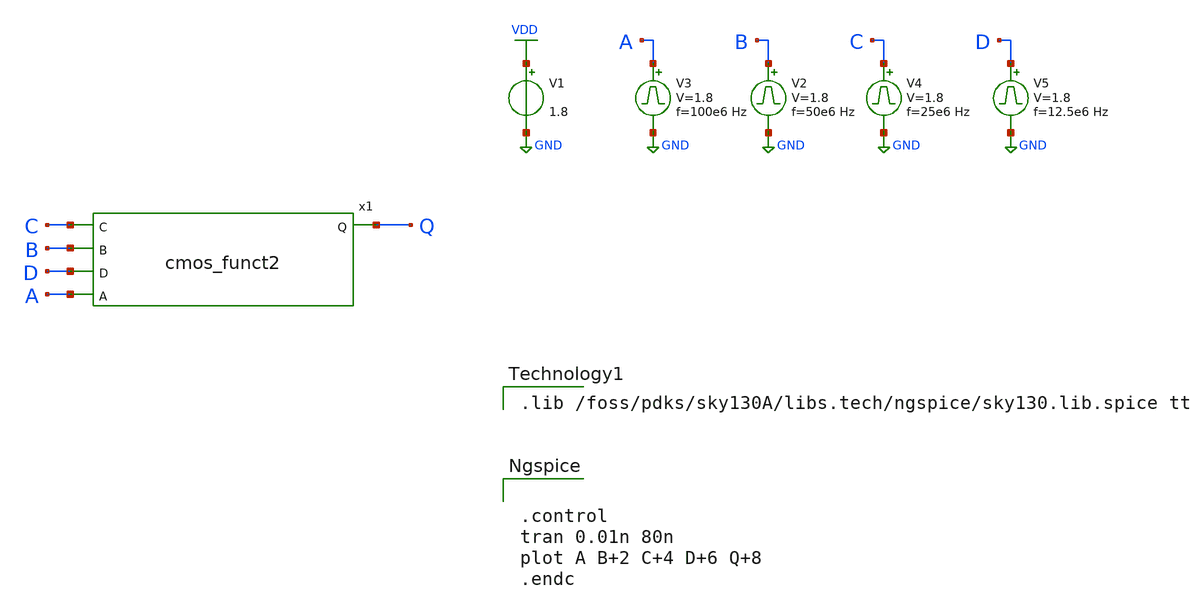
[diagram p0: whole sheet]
** sch_path: Modulo_Digital/Lab1/cmos_funct2_tb.sch
**.subckt cmos_funct2_tb
V1 VDD GND 1.8
V3 A GND pulse 0 1.8 '0.495/ 100e6 ' '0.01/100e6 ' '0.01/100e6 ' '0.49/100e6 ' '1/100e6 '
V2 B GND pulse 0 1.8 '0.495/ 50e6 ' '0.01/50e6 ' '0.01/50e6 ' '0.49/50e6 ' '1/50e6 '
V4 C GND pulse 0 1.8 '0.495/ 25e6 ' '0.01/25e6 ' '0.01/25e6 ' '0.49/25e6 ' '1/25e6 '
V5 D GND pulse 0 1.8 '0.495/ 12.5e6 ' '0.01/12.5e6 ' '0.01/12.5e6 ' '0.49/12.5e6 ' '1/12.5e6 '
x1 C B D A Q cmos_funct2
**** begin user architecture code

.lib /foss/pdks/sky130A/libs.tech/ngspice/sky130.lib.spice tt



.control
tran 0.01n 80n
plot A B+2 C+4 D+6 Q+8
.endc

**** end user architecture code
**.ends
.GLOBAL VDD
.GLOBAL GND
.end
